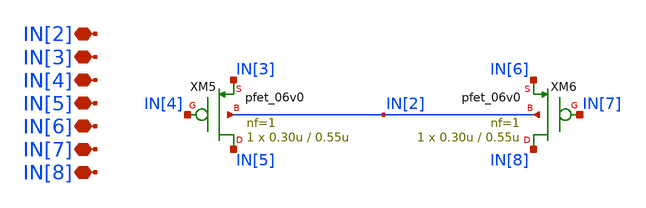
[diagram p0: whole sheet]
** sch_path: designs/libs/core_single-fet/pfet-pin/pfet-pin.sch
**.subckt pfet-pin IN[2] IN[3] IN[4] IN[5] IN[6] IN[7] IN[8]
*.iopin IN[2]
*.iopin IN[3]
*.iopin IN[4]
*.iopin IN[5]
*.iopin IN[6]
*.iopin IN[7]
*.iopin IN[8]
XM5 IN[5] IN[4] IN[3] IN[2] pfet_06v0 L=0.55u W=0.30u nf=1 ad='int((nf+1)/2) * W/nf * 0.18u' as='int((nf+2)/2) * W/nf * 0.18u'
+ pd='2*int((nf+1)/2) * (W/nf + 0.18u)' ps='2*int((nf+2)/2) * (W/nf + 0.18u)' nrd='0.18u / W' nrs='0.18u / W'
+ sa=0 sb=0 sd=0 m=1
XM6 IN[8] IN[7] IN[6] IN[2] pfet_06v0 L=0.55u W=0.30u nf=1 ad='int((nf+1)/2) * W/nf * 0.18u' as='int((nf+2)/2) * W/nf * 0.18u'
+ pd='2*int((nf+1)/2) * (W/nf + 0.18u)' ps='2*int((nf+2)/2) * (W/nf + 0.18u)' nrd='0.18u / W' nrs='0.18u / W'
+ sa=0 sb=0 sd=0 m=1
**.ends
.end
